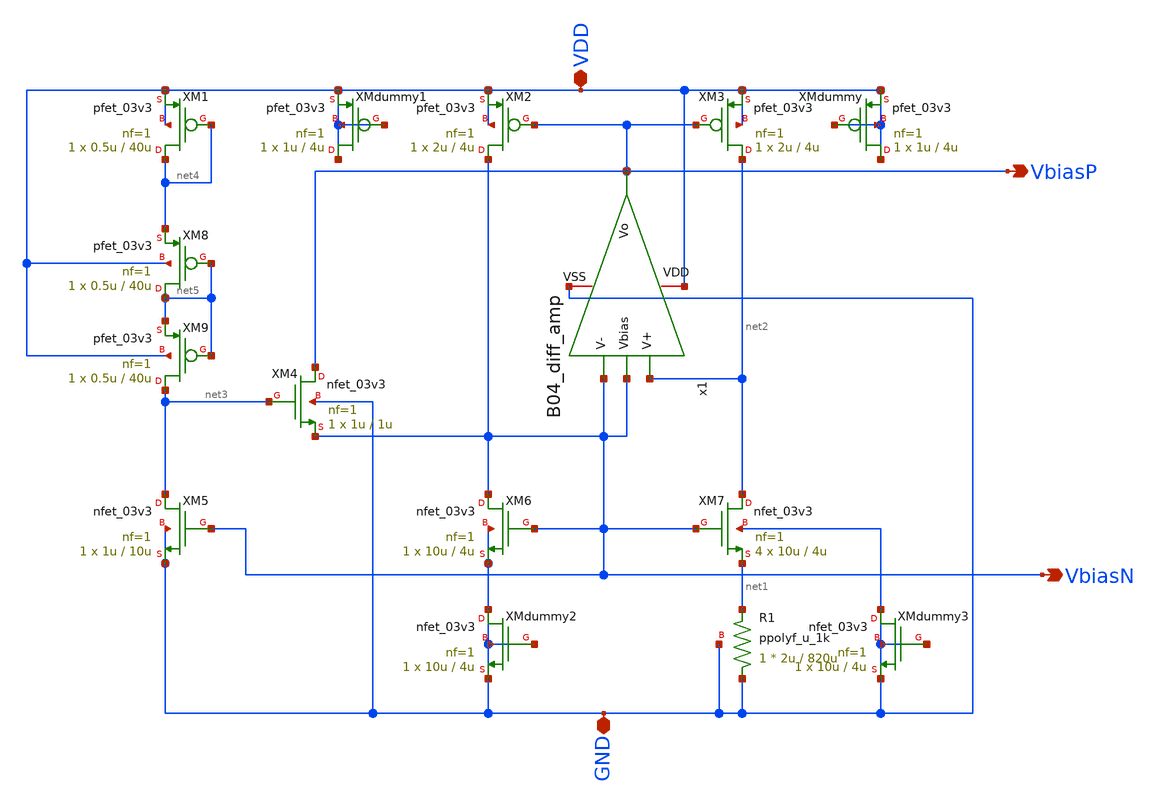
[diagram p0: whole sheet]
** sch_path: analog/B04_BMR.sch
**.subckt B04_BMR VDD GND VbiasP VbiasN
*.iopin VDD
*.iopin GND
*.opin VbiasP
*.opin VbiasN
XM2 VbiasN VbiasP VDD VDD pfet_03v3 L=4u W=2u nf=1 ad='int((nf+1)/2) * W/nf * 0.18u' as='int((nf+2)/2) * W/nf * 0.18u'
+ pd='2*int((nf+1)/2) * (W/nf + 0.18u)' ps='2*int((nf+2)/2) * (W/nf + 0.18u)' nrd='0.18u / W' nrs='0.18u / W'
+ sa=0 sb=0 sd=0 m=1
XM3 net2 VbiasP VDD VDD pfet_03v3 L=4u W=2u nf=1 ad='int((nf+1)/2) * W/nf * 0.18u' as='int((nf+2)/2) * W/nf * 0.18u'
+ pd='2*int((nf+1)/2) * (W/nf + 0.18u)' ps='2*int((nf+2)/2) * (W/nf + 0.18u)' nrd='0.18u / W' nrs='0.18u / W'
+ sa=0 sb=0 sd=0 m=1
XM6 VbiasN VbiasN GND GND nfet_03v3 L=4u W=10u nf=1 ad='int((nf+1)/2) * W/nf * 0.18u' as='int((nf+2)/2) * W/nf * 0.18u'
+ pd='2*int((nf+1)/2) * (W/nf + 0.18u)' ps='2*int((nf+2)/2) * (W/nf + 0.18u)' nrd='0.18u / W' nrs='0.18u / W'
+ sa=0 sb=0 sd=0 m=1
XM7 net2 VbiasN net1 GND nfet_03v3 L=4u W=10u nf=1 ad='int((nf+1)/2) * W/nf * 0.18u' as='int((nf+2)/2) * W/nf * 0.18u'
+ pd='2*int((nf+1)/2) * (W/nf + 0.18u)' ps='2*int((nf+2)/2) * (W/nf + 0.18u)' nrd='0.18u / W' nrs='0.18u / W'
+ sa=0 sb=0 sd=0 m=4
XM1 net4 net4 VDD VDD pfet_03v3 L=40u W=0.5u nf=1 ad='int((nf+1)/2) * W/nf * 0.18u' as='int((nf+2)/2) * W/nf * 0.18u'
+ pd='2*int((nf+1)/2) * (W/nf + 0.18u)' ps='2*int((nf+2)/2) * (W/nf + 0.18u)' nrd='0.18u / W' nrs='0.18u / W'
+ sa=0 sb=0 sd=0 m=1
XM4 VbiasP net3 VbiasN GND nfet_03v3 L=1u W=1u nf=1 ad='int((nf+1)/2) * W/nf * 0.18u' as='int((nf+2)/2) * W/nf * 0.18u'
+ pd='2*int((nf+1)/2) * (W/nf + 0.18u)' ps='2*int((nf+2)/2) * (W/nf + 0.18u)' nrd='0.18u / W' nrs='0.18u / W'
+ sa=0 sb=0 sd=0 m=1
XM5 net3 VbiasN GND GND nfet_03v3 L=10u W=1u nf=1 ad='int((nf+1)/2) * W/nf * 0.18u' as='int((nf+2)/2) * W/nf * 0.18u'
+ pd='2*int((nf+1)/2) * (W/nf + 0.18u)' ps='2*int((nf+2)/2) * (W/nf + 0.18u)' nrd='0.18u / W' nrs='0.18u / W'
+ sa=0 sb=0 sd=0 m=1
XM8 net5 net5 net4 VDD pfet_03v3 L=40u W=0.5u nf=1 ad='int((nf+1)/2) * W/nf * 0.18u' as='int((nf+2)/2) * W/nf * 0.18u'
+ pd='2*int((nf+1)/2) * (W/nf + 0.18u)' ps='2*int((nf+2)/2) * (W/nf + 0.18u)' nrd='0.18u / W' nrs='0.18u / W'
+ sa=0 sb=0 sd=0 m=1
XM9 net3 net5 net5 VDD pfet_03v3 L=40u W=0.5u nf=1 ad='int((nf+1)/2) * W/nf * 0.18u' as='int((nf+2)/2) * W/nf * 0.18u'
+ pd='2*int((nf+1)/2) * (W/nf + 0.18u)' ps='2*int((nf+2)/2) * (W/nf + 0.18u)' nrd='0.18u / W' nrs='0.18u / W'
+ sa=0 sb=0 sd=0 m=1
x1 VDD VbiasP net2 VbiasN VbiasN GND B04_diff_amp
XR1 GND net1 GND ppolyf_u_1k r_width=2u r_length=820u m=1
XMdummy VDD VDD VDD VDD pfet_03v3 L=4u W=1u nf=1 ad='int((nf+1)/2) * W/nf * 0.18u' as='int((nf+2)/2) * W/nf * 0.18u'
+ pd='2*int((nf+1)/2) * (W/nf + 0.18u)' ps='2*int((nf+2)/2) * (W/nf + 0.18u)' nrd='0.18u / W' nrs='0.18u / W'
+ sa=0 sb=0 sd=0 m=1
XMdummy1 VDD VDD VDD VDD pfet_03v3 L=4u W=1u nf=1 ad='int((nf+1)/2) * W/nf * 0.18u' as='int((nf+2)/2) * W/nf * 0.18u'
+ pd='2*int((nf+1)/2) * (W/nf + 0.18u)' ps='2*int((nf+2)/2) * (W/nf + 0.18u)' nrd='0.18u / W' nrs='0.18u / W'
+ sa=0 sb=0 sd=0 m=1
XMdummy2 GND GND GND GND nfet_03v3 L=4u W=10u nf=1 ad='int((nf+1)/2) * W/nf * 0.18u' as='int((nf+2)/2) * W/nf * 0.18u'
+ pd='2*int((nf+1)/2) * (W/nf + 0.18u)' ps='2*int((nf+2)/2) * (W/nf + 0.18u)' nrd='0.18u / W' nrs='0.18u / W'
+ sa=0 sb=0 sd=0 m=1
XMdummy3 GND GND GND GND nfet_03v3 L=4u W=10u nf=1 ad='int((nf+1)/2) * W/nf * 0.18u' as='int((nf+2)/2) * W/nf * 0.18u'
+ pd='2*int((nf+1)/2) * (W/nf + 0.18u)' ps='2*int((nf+2)/2) * (W/nf + 0.18u)' nrd='0.18u / W' nrs='0.18u / W'
+ sa=0 sb=0 sd=0 m=1
**.ends

* expanding   symbol:
*+  AURA-Event-Driven-Mixed-Signal-ASIC-for-Acoustic-Pattern-Detection/analog/B04_diff_amp.sym # of pins=6
** sym_path: analog/B04_diff_amp.sym
** sch_path: analog/B04_diff_amp.sch
.subckt B04_diff_amp VDD Vo V+ V- Vbias VSS
*.iopin VDD
*.iopin VSS
*.ipin V+
*.ipin V-
*.opin Vo
*.ipin Vbias
XM1 net1 V+ net2 VSS nfet_03v3 L=4u W=1.1u nf=1 ad='int((nf+1)/2) * W/nf * 0.18u' as='int((nf+2)/2) * W/nf * 0.18u'
+ pd='2*int((nf+1)/2) * (W/nf + 0.18u)' ps='2*int((nf+2)/2) * (W/nf + 0.18u)' nrd='0.18u / W' nrs='0.18u / W'
+ sa=0 sb=0 sd=0 m=1
XM2 net2 Vbias VSS VSS nfet_03v3 L=4u W=2.2u nf=1 ad='int((nf+1)/2) * W/nf * 0.18u' as='int((nf+2)/2) * W/nf * 0.18u'
+ pd='2*int((nf+1)/2) * (W/nf + 0.18u)' ps='2*int((nf+2)/2) * (W/nf + 0.18u)' nrd='0.18u / W' nrs='0.18u / W'
+ sa=0 sb=0 sd=0 m=1
XM3 Vo V- net2 VSS nfet_03v3 L=4u W=1.1u nf=1 ad='int((nf+1)/2) * W/nf * 0.18u' as='int((nf+2)/2) * W/nf * 0.18u'
+ pd='2*int((nf+1)/2) * (W/nf + 0.18u)' ps='2*int((nf+2)/2) * (W/nf + 0.18u)' nrd='0.18u / W' nrs='0.18u / W'
+ sa=0 sb=0 sd=0 m=1
XM4 Vo net1 VDD VDD pfet_03v3 L=4u W=13u nf=1 ad='int((nf+1)/2) * W/nf * 0.18u' as='int((nf+2)/2) * W/nf * 0.18u'
+ pd='2*int((nf+1)/2) * (W/nf + 0.18u)' ps='2*int((nf+2)/2) * (W/nf + 0.18u)' nrd='0.18u / W' nrs='0.18u / W'
+ sa=0 sb=0 sd=0 m=1
XM5 net1 net1 VDD VDD pfet_03v3 L=4u W=13u nf=1 ad='int((nf+1)/2) * W/nf * 0.18u' as='int((nf+2)/2) * W/nf * 0.18u'
+ pd='2*int((nf+1)/2) * (W/nf + 0.18u)' ps='2*int((nf+2)/2) * (W/nf + 0.18u)' nrd='0.18u / W' nrs='0.18u / W'
+ sa=0 sb=0 sd=0 m=1
XMDummy VDD VDD VDD VDD pfet_03v3 L=4u W=6.5u nf=1 ad='int((nf+1)/2) * W/nf * 0.18u' as='int((nf+2)/2) * W/nf * 0.18u'
+ pd='2*int((nf+1)/2) * (W/nf + 0.18u)' ps='2*int((nf+2)/2) * (W/nf + 0.18u)' nrd='0.18u / W' nrs='0.18u / W'
+ sa=0 sb=0 sd=0 m=1
XMDummy1 VDD VDD VDD VDD pfet_03v3 L=4u W=6.5u nf=1 ad='int((nf+1)/2) * W/nf * 0.18u' as='int((nf+2)/2) * W/nf * 0.18u'
+ pd='2*int((nf+1)/2) * (W/nf + 0.18u)' ps='2*int((nf+2)/2) * (W/nf + 0.18u)' nrd='0.18u / W' nrs='0.18u / W'
+ sa=0 sb=0 sd=0 m=1
XMdummy2 VSS VSS VSS VSS nfet_03v3 L=4u W=0.55u nf=1 ad='int((nf+1)/2) * W/nf * 0.18u' as='int((nf+2)/2) * W/nf * 0.18u'
+ pd='2*int((nf+1)/2) * (W/nf + 0.18u)' ps='2*int((nf+2)/2) * (W/nf + 0.18u)' nrd='0.18u / W' nrs='0.18u / W'
+ sa=0 sb=0 sd=0 m=1
XMdummy3 VSS VSS VSS VSS nfet_03v3 L=4u W=0.55u nf=1 ad='int((nf+1)/2) * W/nf * 0.18u' as='int((nf+2)/2) * W/nf * 0.18u'
+ pd='2*int((nf+1)/2) * (W/nf + 0.18u)' ps='2*int((nf+2)/2) * (W/nf + 0.18u)' nrd='0.18u / W' nrs='0.18u / W'
+ sa=0 sb=0 sd=0 m=1
.ends

.end
